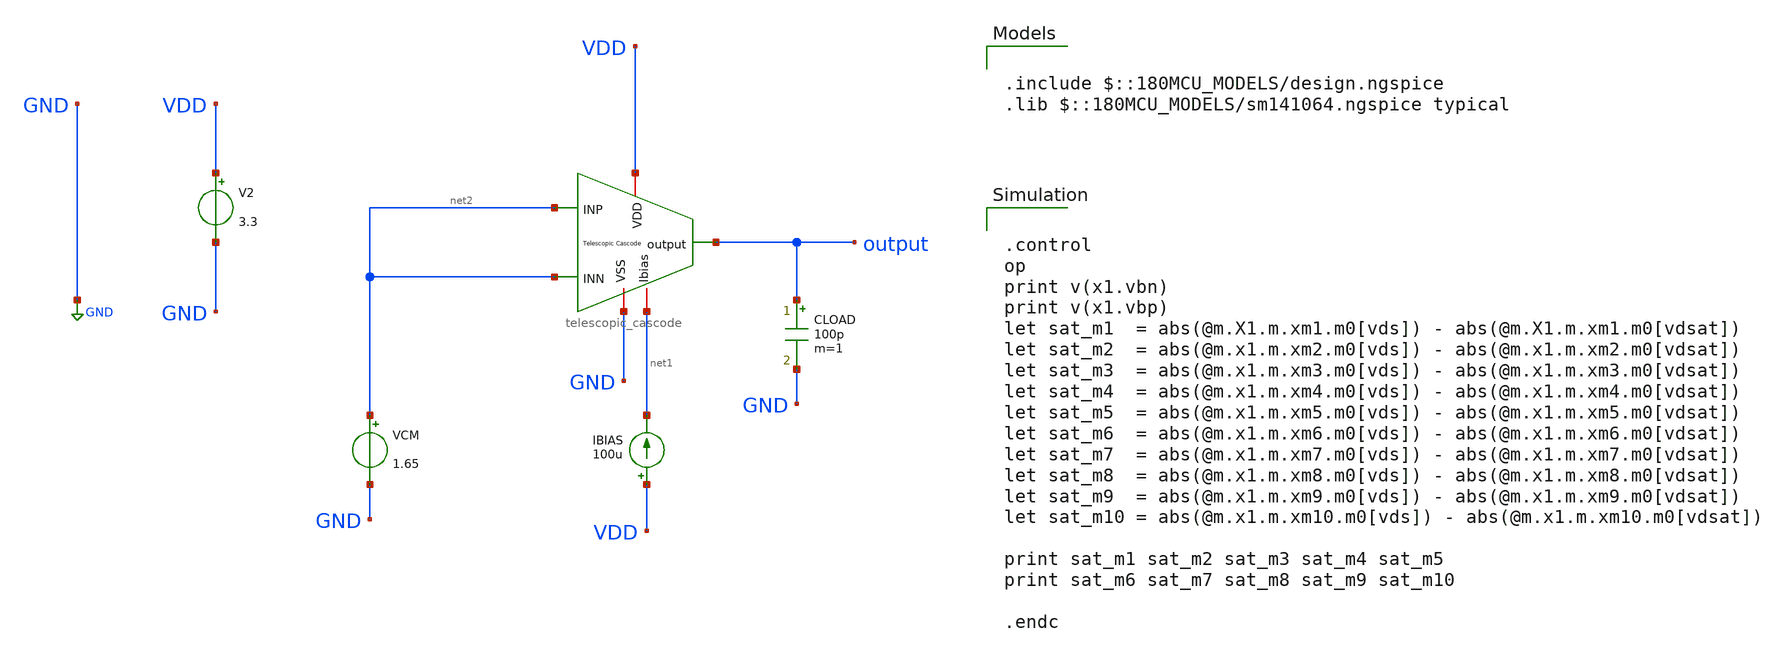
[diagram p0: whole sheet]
** sch_path: designs/libs/core_amps/ota_telescopic/tb/telescopic_vdsat_tb.sch
**.subckt telescopic_vdsat_tb
IBIAS VDD net1 100u
V2 VDD GND 3.3
CLOAD output GND 100p m=1
VCM net2 GND 1.65
x1 VDD output net2 net2 GND net1 telescopic_cascode
**** begin user architecture code

.include $::180MCU_MODELS/design.ngspice
.lib $::180MCU_MODELS/sm141064.ngspice typical



.control
op
print v(x1.vbn)
print v(x1.vbp)
let sat_m1  = abs(@m.X1.m.xm1.m0[vds]) - abs(@m.X1.m.xm1.m0[vdsat])
let sat_m2  = abs(@m.x1.m.xm2.m0[vds]) - abs(@m.x1.m.xm2.m0[vdsat])
let sat_m3  = abs(@m.x1.m.xm3.m0[vds]) - abs(@m.x1.m.xm3.m0[vdsat])
let sat_m4  = abs(@m.x1.m.xm4.m0[vds]) - abs(@m.x1.m.xm4.m0[vdsat])
let sat_m5  = abs(@m.x1.m.xm5.m0[vds]) - abs(@m.x1.m.xm5.m0[vdsat])
let sat_m6  = abs(@m.x1.m.xm6.m0[vds]) - abs(@m.x1.m.xm6.m0[vdsat])
let sat_m7  = abs(@m.x1.m.xm7.m0[vds]) - abs(@m.x1.m.xm7.m0[vdsat])
let sat_m8  = abs(@m.x1.m.xm8.m0[vds]) - abs(@m.x1.m.xm8.m0[vdsat])
let sat_m9  = abs(@m.x1.m.xm9.m0[vds]) - abs(@m.x1.m.xm9.m0[vdsat])
let sat_m10 = abs(@m.x1.m.xm10.m0[vds]) - abs(@m.x1.m.xm10.m0[vdsat])

print sat_m1 sat_m2 sat_m3 sat_m4 sat_m5
print sat_m6 sat_m7 sat_m8 sat_m9 sat_m10

.endc



**** end user architecture code
**.ends
.GLOBAL GND
.end
